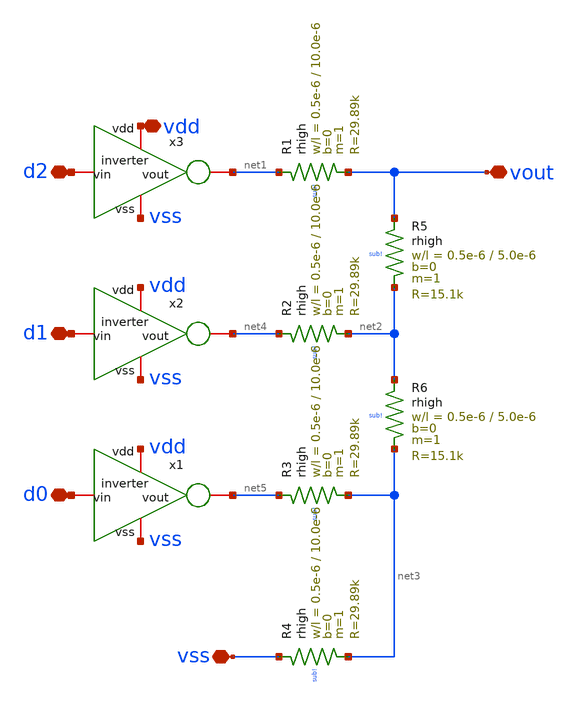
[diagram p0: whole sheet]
** sch_path: xschem/rdac.sch
**.subckt rdac vout vdd d0 vss d1 d2
*.iopin vout
*.iopin vdd
*.iopin d0
*.iopin vss
*.iopin d1
*.iopin d2
x1 vdd d0 net5 vss inverter
x2 vdd d1 net4 vss inverter
x3 vdd d2 net1 vss inverter
XR1 net1 vout sub! rhigh w=0.5e-6 l=10.0e-6 m=1 b=0 mm_ok=1
XR2 net4 net2 sub! rhigh w=0.5e-6 l=10.0e-6 m=1 b=0 mm_ok=1
XR3 net5 net3 sub! rhigh w=0.5e-6 l=10.0e-6 m=1 b=0 mm_ok=1
XR4 vss net3 sub! rhigh w=0.5e-6 l=10.0e-6 m=1 b=0 mm_ok=1
XR5 vout net2 sub! rhigh w=0.5e-6 l=5.0e-6 m=1 b=0 mm_ok=1
XR6 net2 net3 sub! rhigh w=0.5e-6 l=5.0e-6 m=1 b=0 mm_ok=1
**.ends

* expanding   symbol:  inverter.sym # of pins=4
** sym_path: xschem/inverter.sym
** sch_path: xschem/inverter.sch
.subckt inverter vdd vin vout vss
*.iopin vout
*.iopin vss
*.iopin vin
*.iopin vdd
XM1 vout vin vss vss sg13_lv_nmos w=1.5u l=0.13u ng=1 m=1 mm_ok=1
XM2 vout vin vdd vdd sg13_lv_pmos w=3.0u l=0.13u ng=1 m=1 mm_ok=1
.ends

.end
